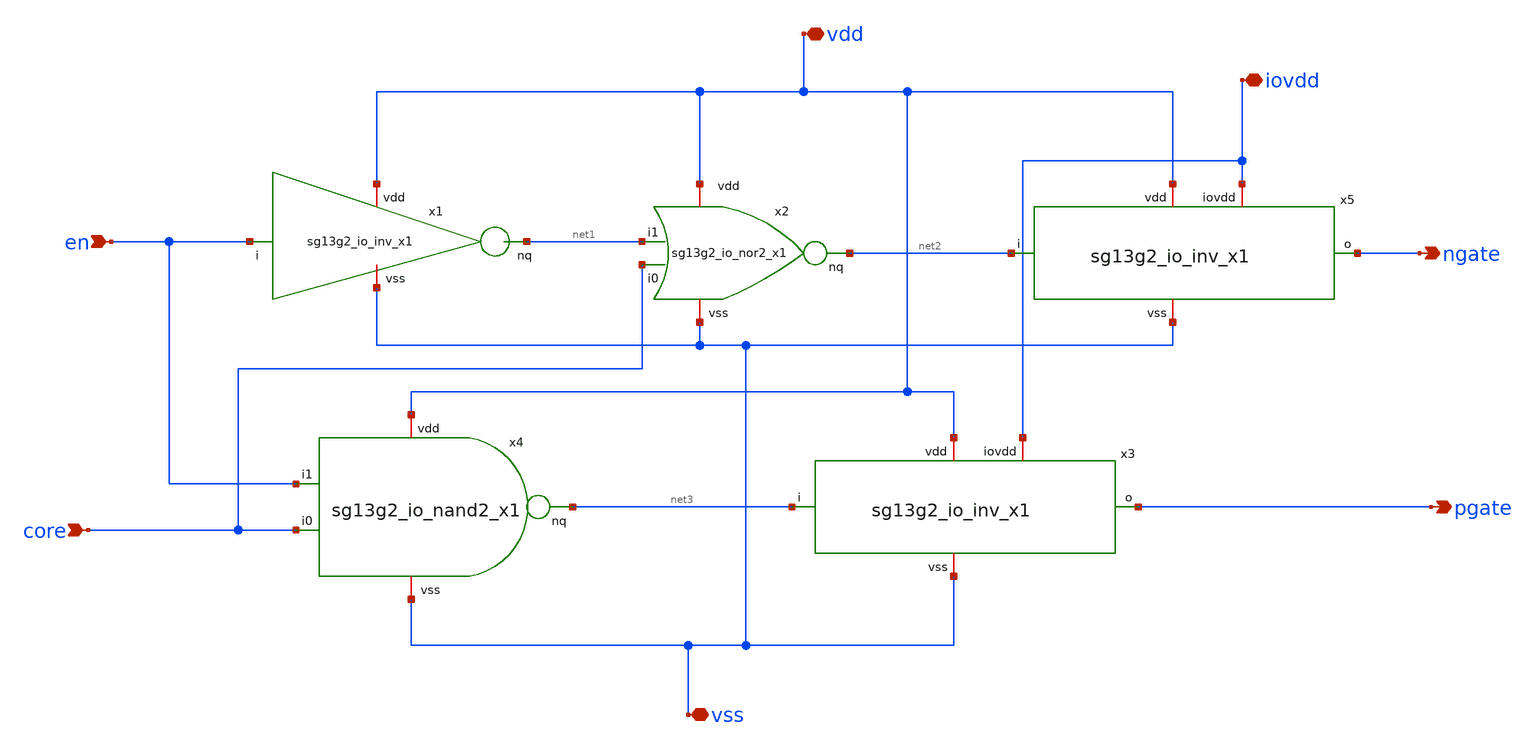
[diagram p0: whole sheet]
** sch_path: CDR4176-main/schematic/xschem/project_io/sg13g2_GateDecode/sg13g2_GateDecode.sch
**.subckt sg13g2_GateDecode en core vss vdd iovdd ngate pgate
*.ipin en
*.ipin core
*.iopin vss
*.iopin vdd
*.iopin iovdd
*.opin ngate
*.opin pgate
x1 vdd en net1 vss sg13g2_io_inv_x1
x2 vdd core net2 net1 vss sg13g2_io_nor2_x1
x3 iovdd vdd net3 pgate vss sg13g2_LevelUp
x4 vdd net3 en core vss sg13g2_io_nand2_x1
x5 iovdd vdd net2 ngate vss sg13g2_LevelUp
**.ends
.end
